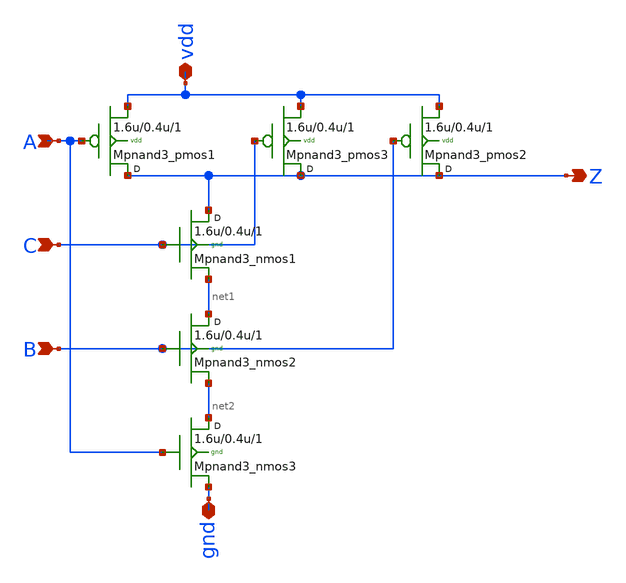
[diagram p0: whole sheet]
** sch_path: sram_4_16_scn4m/pnand3_0.sch
**.subckt pnand3_0 C A B Z vdd gnd
*.ipin C
*.ipin A
*.ipin B
*.opin Z
*.iopin vdd
*.iopin gnd
Mpnand3_nmos1 Z C net1 gnd n w=1.6u l=0.4u m=1
Mpnand3_pmos1 Z A vdd vdd p w=1.6u l=0.4u m=1
Mpnand3_pmos3 Z C vdd vdd p w=1.6u l=0.4u m=1
Mpnand3_nmos2 net1 B net2 gnd n w=1.6u l=0.4u m=1
Mpnand3_pmos2 Z B vdd vdd p w=1.6u l=0.4u m=1
Mpnand3_nmos3 net2 A gnd gnd n w=1.6u l=0.4u m=1
**.ends
.end
